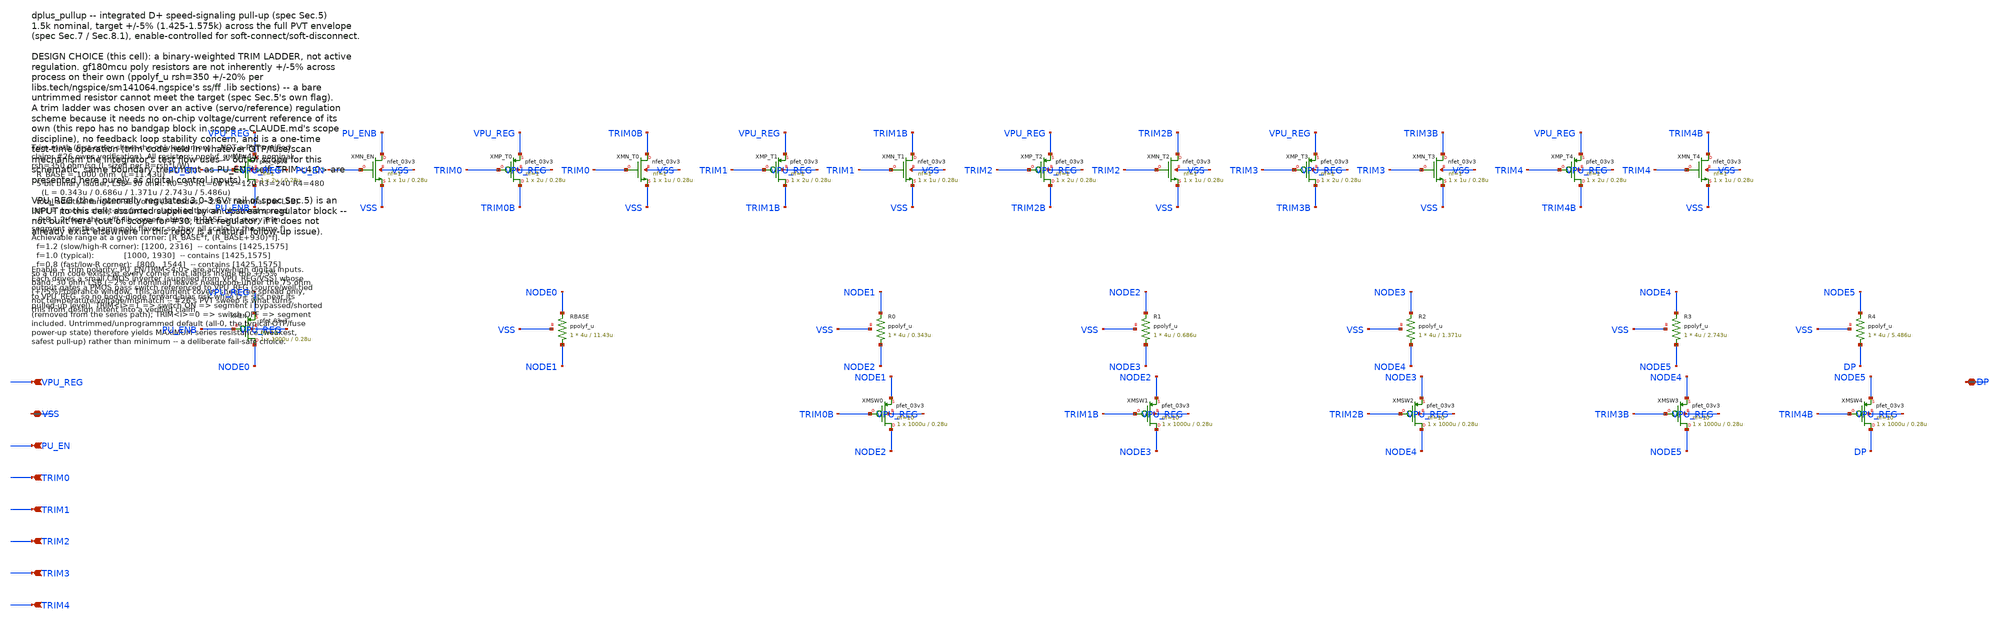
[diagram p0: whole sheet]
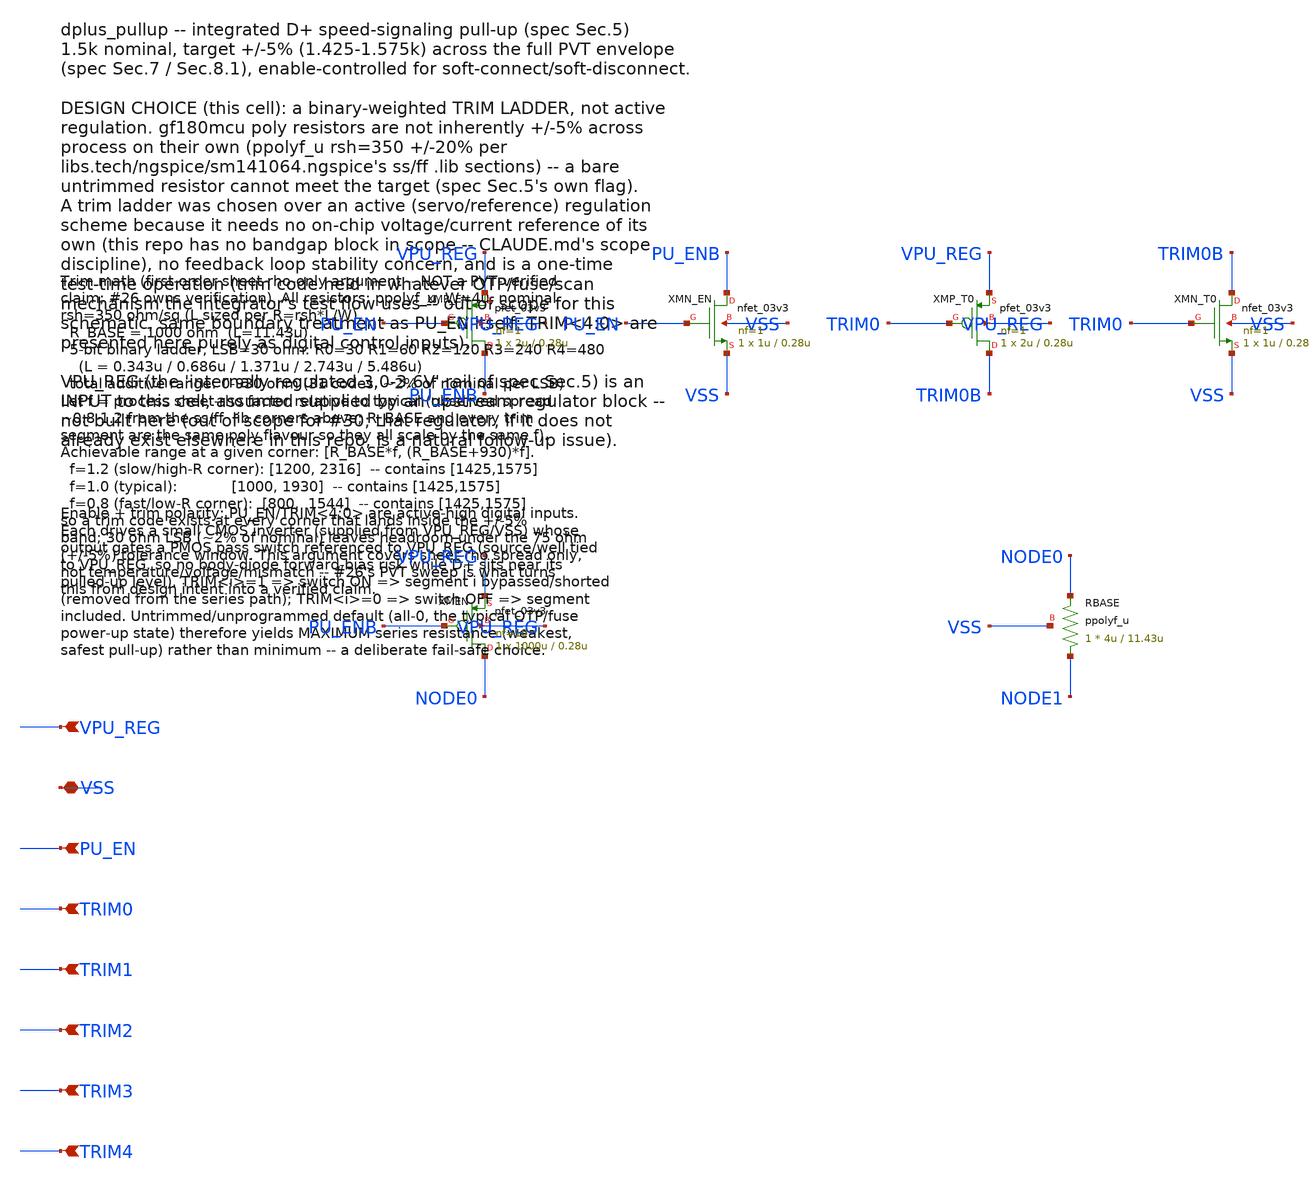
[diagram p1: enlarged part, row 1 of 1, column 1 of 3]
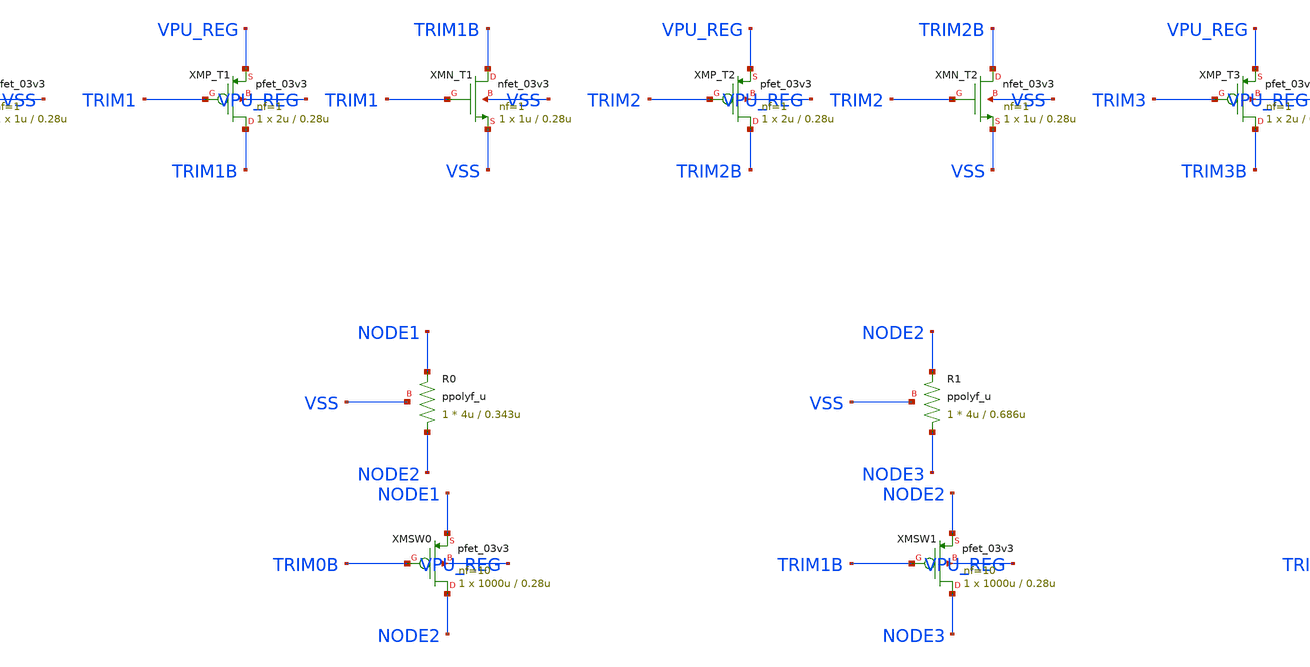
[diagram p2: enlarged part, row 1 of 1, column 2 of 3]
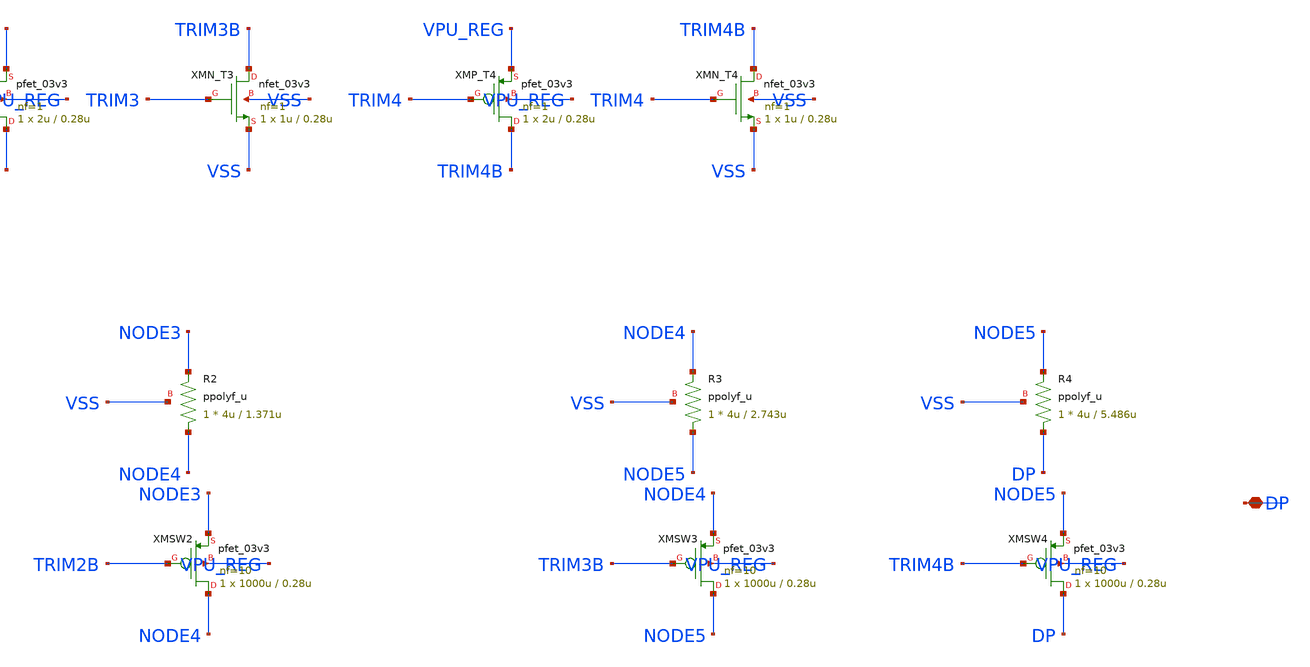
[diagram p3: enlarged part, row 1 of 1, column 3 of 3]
** sch_path: design/dplus_pullup.sch
**.subckt dplus_pullup DP VPU_REG VSS PU_EN TRIM0 TRIM1 TRIM2 TRIM3 TRIM4
*.iopin DP
*.ipin VPU_REG
*.iopin VSS
*.ipin PU_EN
*.ipin TRIM0
*.ipin TRIM1
*.ipin TRIM2
*.ipin TRIM3
*.ipin TRIM4
XMP_EN PU_ENB PU_EN VPU_REG VPU_REG pfet_03v3 L=0.28u W=2u nf=1 ad='int((nf+1)/2) * W/nf * 0.18u' as='int((nf+2)/2) * W/nf * 0.18u'
+ pd='2*int((nf+1)/2) * (W/nf + 0.18u)' ps='2*int((nf+2)/2) * (W/nf + 0.18u)' nrd='0.18u / W' nrs='0.18u / W'
+ sa=0 sb=0 sd=0 m=1
XMN_EN PU_ENB PU_EN VSS VSS nfet_03v3 L=0.28u W=1u nf=1 ad='int((nf+1)/2) * W/nf * 0.18u' as='int((nf+2)/2) * W/nf * 0.18u'
+ pd='2*int((nf+1)/2) * (W/nf + 0.18u)' ps='2*int((nf+2)/2) * (W/nf + 0.18u)' nrd='0.18u / W' nrs='0.18u / W'
+ sa=0 sb=0 sd=0 m=1
XMP_T0 TRIM0B TRIM0 VPU_REG VPU_REG pfet_03v3 L=0.28u W=2u nf=1 ad='int((nf+1)/2) * W/nf * 0.18u' as='int((nf+2)/2) * W/nf * 0.18u'
+ pd='2*int((nf+1)/2) * (W/nf + 0.18u)' ps='2*int((nf+2)/2) * (W/nf + 0.18u)' nrd='0.18u / W' nrs='0.18u / W'
+ sa=0 sb=0 sd=0 m=1
XMN_T0 TRIM0B TRIM0 VSS VSS nfet_03v3 L=0.28u W=1u nf=1 ad='int((nf+1)/2) * W/nf * 0.18u' as='int((nf+2)/2) * W/nf * 0.18u'
+ pd='2*int((nf+1)/2) * (W/nf + 0.18u)' ps='2*int((nf+2)/2) * (W/nf + 0.18u)' nrd='0.18u / W' nrs='0.18u / W'
+ sa=0 sb=0 sd=0 m=1
XMP_T1 TRIM1B TRIM1 VPU_REG VPU_REG pfet_03v3 L=0.28u W=2u nf=1 ad='int((nf+1)/2) * W/nf * 0.18u' as='int((nf+2)/2) * W/nf * 0.18u'
+ pd='2*int((nf+1)/2) * (W/nf + 0.18u)' ps='2*int((nf+2)/2) * (W/nf + 0.18u)' nrd='0.18u / W' nrs='0.18u / W'
+ sa=0 sb=0 sd=0 m=1
XMN_T1 TRIM1B TRIM1 VSS VSS nfet_03v3 L=0.28u W=1u nf=1 ad='int((nf+1)/2) * W/nf * 0.18u' as='int((nf+2)/2) * W/nf * 0.18u'
+ pd='2*int((nf+1)/2) * (W/nf + 0.18u)' ps='2*int((nf+2)/2) * (W/nf + 0.18u)' nrd='0.18u / W' nrs='0.18u / W'
+ sa=0 sb=0 sd=0 m=1
XMP_T2 TRIM2B TRIM2 VPU_REG VPU_REG pfet_03v3 L=0.28u W=2u nf=1 ad='int((nf+1)/2) * W/nf * 0.18u' as='int((nf+2)/2) * W/nf * 0.18u'
+ pd='2*int((nf+1)/2) * (W/nf + 0.18u)' ps='2*int((nf+2)/2) * (W/nf + 0.18u)' nrd='0.18u / W' nrs='0.18u / W'
+ sa=0 sb=0 sd=0 m=1
XMN_T2 TRIM2B TRIM2 VSS VSS nfet_03v3 L=0.28u W=1u nf=1 ad='int((nf+1)/2) * W/nf * 0.18u' as='int((nf+2)/2) * W/nf * 0.18u'
+ pd='2*int((nf+1)/2) * (W/nf + 0.18u)' ps='2*int((nf+2)/2) * (W/nf + 0.18u)' nrd='0.18u / W' nrs='0.18u / W'
+ sa=0 sb=0 sd=0 m=1
XMP_T3 TRIM3B TRIM3 VPU_REG VPU_REG pfet_03v3 L=0.28u W=2u nf=1 ad='int((nf+1)/2) * W/nf * 0.18u' as='int((nf+2)/2) * W/nf * 0.18u'
+ pd='2*int((nf+1)/2) * (W/nf + 0.18u)' ps='2*int((nf+2)/2) * (W/nf + 0.18u)' nrd='0.18u / W' nrs='0.18u / W'
+ sa=0 sb=0 sd=0 m=1
XMN_T3 TRIM3B TRIM3 VSS VSS nfet_03v3 L=0.28u W=1u nf=1 ad='int((nf+1)/2) * W/nf * 0.18u' as='int((nf+2)/2) * W/nf * 0.18u'
+ pd='2*int((nf+1)/2) * (W/nf + 0.18u)' ps='2*int((nf+2)/2) * (W/nf + 0.18u)' nrd='0.18u / W' nrs='0.18u / W'
+ sa=0 sb=0 sd=0 m=1
XMP_T4 TRIM4B TRIM4 VPU_REG VPU_REG pfet_03v3 L=0.28u W=2u nf=1 ad='int((nf+1)/2) * W/nf * 0.18u' as='int((nf+2)/2) * W/nf * 0.18u'
+ pd='2*int((nf+1)/2) * (W/nf + 0.18u)' ps='2*int((nf+2)/2) * (W/nf + 0.18u)' nrd='0.18u / W' nrs='0.18u / W'
+ sa=0 sb=0 sd=0 m=1
XMN_T4 TRIM4B TRIM4 VSS VSS nfet_03v3 L=0.28u W=1u nf=1 ad='int((nf+1)/2) * W/nf * 0.18u' as='int((nf+2)/2) * W/nf * 0.18u'
+ pd='2*int((nf+1)/2) * (W/nf + 0.18u)' ps='2*int((nf+2)/2) * (W/nf + 0.18u)' nrd='0.18u / W' nrs='0.18u / W'
+ sa=0 sb=0 sd=0 m=1
XMEN NODE0 PU_ENB VPU_REG VPU_REG pfet_03v3 L=0.28u W=1000u nf=10 ad='int((nf+1)/2) * W/nf * 0.18u' as='int((nf+2)/2) * W/nf * 0.18u'
+ pd='2*int((nf+1)/2) * (W/nf + 0.18u)' ps='2*int((nf+2)/2) * (W/nf + 0.18u)' nrd='0.18u / W' nrs='0.18u / W'
+ sa=0 sb=0 sd=0 m=1
XRBASE NODE1 NODE0 VSS ppolyf_u r_width=4u r_length=11.43u m=1
XR0 NODE2 NODE1 VSS ppolyf_u r_width=4u r_length=0.343u m=1
XMSW0 NODE2 TRIM0B NODE1 VPU_REG pfet_03v3 L=0.28u W=1000u nf=10 ad='int((nf+1)/2) * W/nf * 0.18u' as='int((nf+2)/2) * W/nf * 0.18u'
+ pd='2*int((nf+1)/2) * (W/nf + 0.18u)' ps='2*int((nf+2)/2) * (W/nf + 0.18u)' nrd='0.18u / W' nrs='0.18u / W'
+ sa=0 sb=0 sd=0 m=1
XR1 NODE3 NODE2 VSS ppolyf_u r_width=4u r_length=0.686u m=1
XMSW1 NODE3 TRIM1B NODE2 VPU_REG pfet_03v3 L=0.28u W=1000u nf=10 ad='int((nf+1)/2) * W/nf * 0.18u' as='int((nf+2)/2) * W/nf * 0.18u'
+ pd='2*int((nf+1)/2) * (W/nf + 0.18u)' ps='2*int((nf+2)/2) * (W/nf + 0.18u)' nrd='0.18u / W' nrs='0.18u / W'
+ sa=0 sb=0 sd=0 m=1
XR2 NODE4 NODE3 VSS ppolyf_u r_width=4u r_length=1.371u m=1
XMSW2 NODE4 TRIM2B NODE3 VPU_REG pfet_03v3 L=0.28u W=1000u nf=10 ad='int((nf+1)/2) * W/nf * 0.18u' as='int((nf+2)/2) * W/nf * 0.18u'
+ pd='2*int((nf+1)/2) * (W/nf + 0.18u)' ps='2*int((nf+2)/2) * (W/nf + 0.18u)' nrd='0.18u / W' nrs='0.18u / W'
+ sa=0 sb=0 sd=0 m=1
XR3 NODE5 NODE4 VSS ppolyf_u r_width=4u r_length=2.743u m=1
XMSW3 NODE5 TRIM3B NODE4 VPU_REG pfet_03v3 L=0.28u W=1000u nf=10 ad='int((nf+1)/2) * W/nf * 0.18u' as='int((nf+2)/2) * W/nf * 0.18u'
+ pd='2*int((nf+1)/2) * (W/nf + 0.18u)' ps='2*int((nf+2)/2) * (W/nf + 0.18u)' nrd='0.18u / W' nrs='0.18u / W'
+ sa=0 sb=0 sd=0 m=1
XR4 DP NODE5 VSS ppolyf_u r_width=4u r_length=5.486u m=1
XMSW4 DP TRIM4B NODE5 VPU_REG pfet_03v3 L=0.28u W=1000u nf=10 ad='int((nf+1)/2) * W/nf * 0.18u' as='int((nf+2)/2) * W/nf * 0.18u'
+ pd='2*int((nf+1)/2) * (W/nf + 0.18u)' ps='2*int((nf+2)/2) * (W/nf + 0.18u)' nrd='0.18u / W' nrs='0.18u / W'
+ sa=0 sb=0 sd=0 m=1
**.ends
.end
